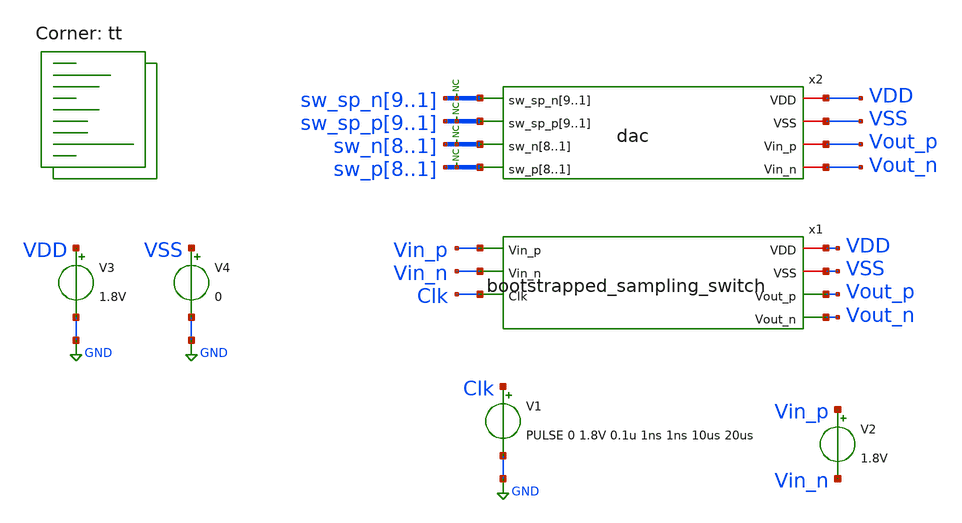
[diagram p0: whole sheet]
** sch_path: xschem/tests/bootstrapped_sampling_switch/bootstrapped_sampling_switch_w_caps_test.sch
**.subckt bootstrapped_sampling_switch_w_caps_test
V3 VDD GND 1.8V
V4 VSS GND 0
x1 VDD Vin_p VSS Vin_n Clk Vout_p Vout_n bootstrapped_sampling_switch
V2 Vin_p Vin_n 1.8V
x2 sw_sp_n9 sw_sp_n8 sw_sp_n7 sw_sp_n6 sw_sp_n5 sw_sp_n4 sw_sp_n3 sw_sp_n2 sw_sp_n1 VDD sw_sp_p9
+ sw_sp_p8 sw_sp_p7 sw_sp_p6 sw_sp_p5 sw_sp_p4 sw_sp_p3 sw_sp_p2 sw_sp_p1 VSS sw_n8 sw_n7 sw_n6 sw_n5 sw_n4
+ sw_n3 sw_n2 sw_n1 Vout_p sw_p8 sw_p7 sw_p6 sw_p5 sw_p4 sw_p3 sw_p2 sw_p1 Vout_n dac
V1 Clk GND PULSE 0 1.8V 0.1u 1ns 1ns 10us 20us
* noconn sw_sp_n[9..1]
* noconn sw_sp_p[9..1]
* noconn sw_n[8..1]
* noconn sw_p[8..1]
**** begin user architecture code
 *.lib $::SKYWATER_MODELS/sky130.lib.spice tt
.include $::SKYWATER_STDCELLS/sky130_fd_sc_hd.spice


.options acct list
.temp 25
*vvcc VDD 0 dc 1.8
*vvss VSS 0 0

v_sp_n1 sw_sp_n1 gnd 1.8V
v_sp_n2 sw_sp_n2 gnd 1.8V
v_sp_n3 sw_sp_n3 gnd 1.8V
v_sp_n4 sw_sp_n4 gnd 1.8V
v_sp_n5 sw_sp_n5 gnd 1.8V
v_sp_n6 sw_sp_n6 gnd 1.8V
v_sp_n7 sw_sp_n7 gnd 1.8V
v_sp_n8 sw_sp_n8 gnd 1.8V
v_sp_n9 sw_sp_n9 gnd 1.8V

v_n1 sw_n1 gnd 0
v_n2 sw_n2 gnd 0
v_n3 sw_n3 gnd 0
v_n4 sw_n4 gnd 0
v_n5 sw_n5 gnd 0
v_n6 sw_n6 gnd 0
v_n7 sw_n7 gnd 0
v_n8 sw_n8 gnd 0

v_sp_p1 sw_sp_p1 gnd 1.8V
v_sp_p2 sw_sp_p2 gnd 1.8V
v_sp_p3 sw_sp_p3 gnd 1.8V
v_sp_p4 sw_sp_p4 gnd 1.8V
v_sp_p5 sw_sp_p5 gnd 1.8V
v_sp_p6 sw_sp_p6 gnd 1.8V
v_sp_p7 sw_sp_p7 gnd 1.8V
v_sp_p8 sw_sp_p8 gnd 1.8V
v_sp_p9 sw_sp_p9 gnd 1.8V

v_p1 sw_p1 gnd 0
v_p2 sw_p2 gnd 0
v_p3 sw_p3 gnd 0
v_p4 sw_p4 gnd 0
v_p5 sw_p5 gnd 0
v_p6 sw_p6 gnd 0
v_p7 sw_p7 gnd 0
v_p8 sw_p8 gnd 0
.control
save all
tran 0.5n 0.3u
*plot RST_PLS clk+2 Pulse+4
plot Vout_p-Vout_n clk-4
write bootstrapped_sampling_switch_w_caps_test.raw
.endc


.lib $::SKYWATER_MODELS/sky130.lib.spice tt
**** end user architecture code
**.ends
.GLOBAL GND
.end
